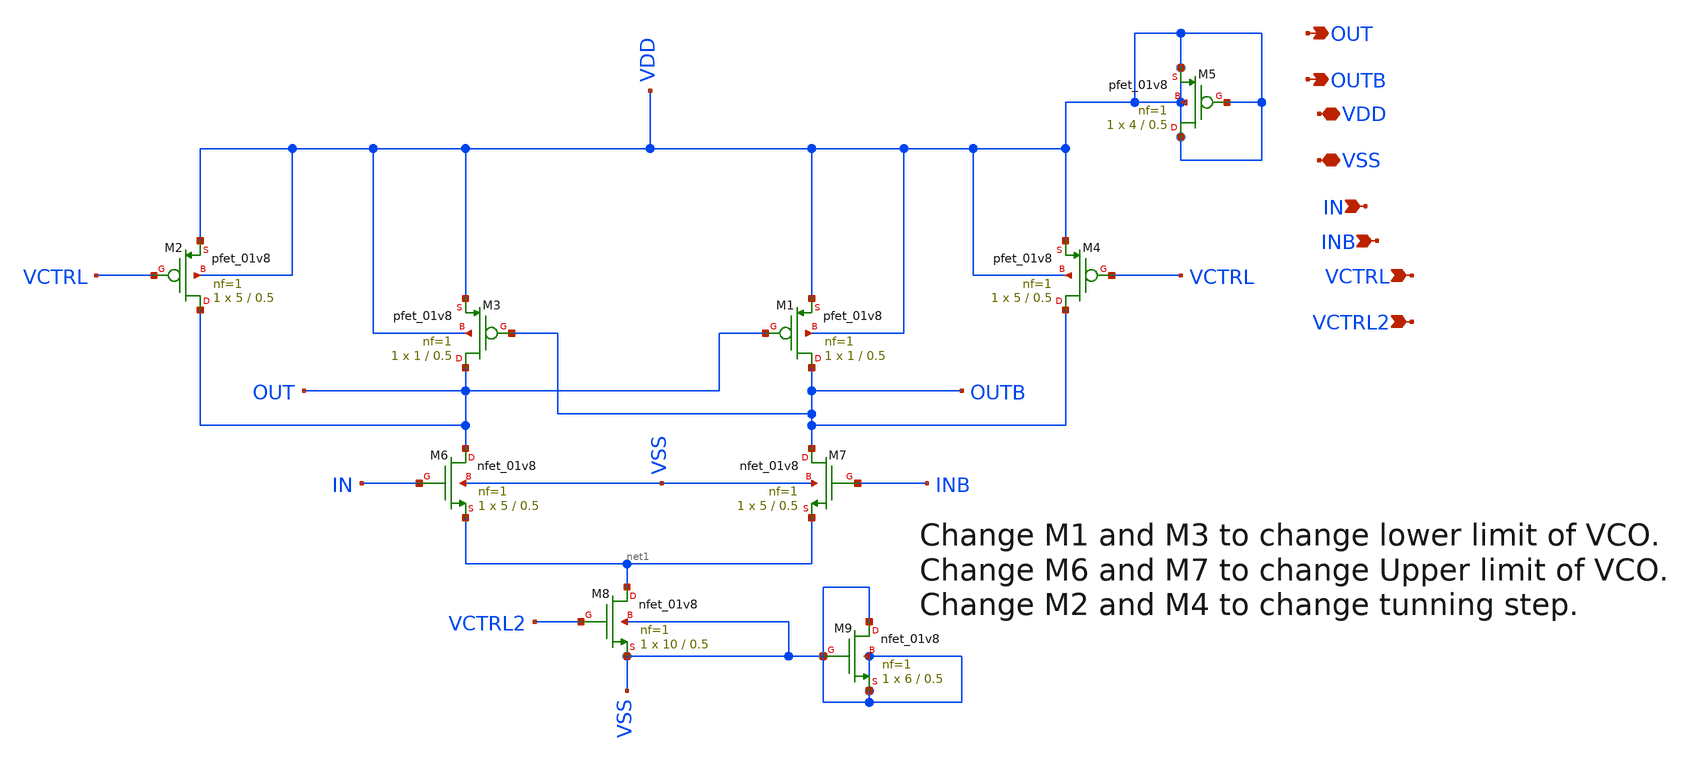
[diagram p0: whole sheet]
** sch_path: Xschem/PLL_TOP_Schematics/DelayCell_1.sch
**.subckt DelayCell_1 VDD VSS IN INB VCTRL VCTRL2 OUT OUTB
*.iopin VDD
*.iopin VSS
*.ipin IN
*.ipin INB
*.ipin VCTRL
*.ipin VCTRL2
*.opin OUT
*.opin OUTB
XM1 OUTB OUT VDD VDD sky130_fd_pr__pfet_01v8 L=0.5 W=1 nf=1 ad='int((nf+1)/2) * W/nf * 0.29' as='int((nf+2)/2) * W/nf * 0.29'
+ pd='2*int((nf+1)/2) * (W/nf + 0.29)' ps='2*int((nf+2)/2) * (W/nf + 0.29)' nrd='0.29 / W' nrs='0.29 / W'
+ sa=0 sb=0 sd=0 mult=1 m=1
XM2 OUT VCTRL VDD VDD sky130_fd_pr__pfet_01v8 L=0.5 W=5 nf=1 ad='int((nf+1)/2) * W/nf * 0.29' as='int((nf+2)/2) * W/nf * 0.29'
+ pd='2*int((nf+1)/2) * (W/nf + 0.29)' ps='2*int((nf+2)/2) * (W/nf + 0.29)' nrd='0.29 / W' nrs='0.29 / W'
+ sa=0 sb=0 sd=0 mult=1 m=1
XM3 OUT OUTB VDD VDD sky130_fd_pr__pfet_01v8 L=0.5 W=1 nf=1 ad='int((nf+1)/2) * W/nf * 0.29' as='int((nf+2)/2) * W/nf * 0.29'
+ pd='2*int((nf+1)/2) * (W/nf + 0.29)' ps='2*int((nf+2)/2) * (W/nf + 0.29)' nrd='0.29 / W' nrs='0.29 / W'
+ sa=0 sb=0 sd=0 mult=1 m=1
XM4 OUTB VCTRL VDD VDD sky130_fd_pr__pfet_01v8 L=0.5 W=5 nf=1 ad='int((nf+1)/2) * W/nf * 0.29' as='int((nf+2)/2) * W/nf * 0.29'
+ pd='2*int((nf+1)/2) * (W/nf + 0.29)' ps='2*int((nf+2)/2) * (W/nf + 0.29)' nrd='0.29 / W' nrs='0.29 / W'
+ sa=0 sb=0 sd=0 mult=1 m=1
XM6 OUT IN net1 VSS sky130_fd_pr__nfet_01v8 L=0.5 W=5 nf=1 ad='int((nf+1)/2) * W/nf * 0.29' as='int((nf+2)/2) * W/nf * 0.29'
+ pd='2*int((nf+1)/2) * (W/nf + 0.29)' ps='2*int((nf+2)/2) * (W/nf + 0.29)' nrd='0.29 / W' nrs='0.29 / W'
+ sa=0 sb=0 sd=0 mult=1 m=1
XM7 OUTB INB net1 VSS sky130_fd_pr__nfet_01v8 L=0.5 W=5 nf=1 ad='int((nf+1)/2) * W/nf * 0.29' as='int((nf+2)/2) * W/nf * 0.29'
+ pd='2*int((nf+1)/2) * (W/nf + 0.29)' ps='2*int((nf+2)/2) * (W/nf + 0.29)' nrd='0.29 / W' nrs='0.29 / W'
+ sa=0 sb=0 sd=0 mult=1 m=1
XM8 net1 VCTRL2 VSS VSS sky130_fd_pr__nfet_01v8 L=0.5 W=10 nf=1 ad='int((nf+1)/2) * W/nf * 0.29' as='int((nf+2)/2) * W/nf * 0.29'
+ pd='2*int((nf+1)/2) * (W/nf + 0.29)' ps='2*int((nf+2)/2) * (W/nf + 0.29)' nrd='0.29 / W' nrs='0.29 / W'
+ sa=0 sb=0 sd=0 mult=1 m=1
XM5 VDD VDD VDD VDD sky130_fd_pr__pfet_01v8 L=0.5 W=4 nf=1 ad='int((nf+1)/2) * W/nf * 0.29' as='int((nf+2)/2) * W/nf * 0.29'
+ pd='2*int((nf+1)/2) * (W/nf + 0.29)' ps='2*int((nf+2)/2) * (W/nf + 0.29)' nrd='0.29 / W' nrs='0.29 / W'
+ sa=0 sb=0 sd=0 mult=1 m=1
XM9 VSS VSS VSS VSS sky130_fd_pr__nfet_01v8 L=0.5 W=6 nf=1 ad='int((nf+1)/2) * W/nf * 0.29' as='int((nf+2)/2) * W/nf * 0.29'
+ pd='2*int((nf+1)/2) * (W/nf + 0.29)' ps='2*int((nf+2)/2) * (W/nf + 0.29)' nrd='0.29 / W' nrs='0.29 / W'
+ sa=0 sb=0 sd=0 mult=1 m=1
**.ends
.end
